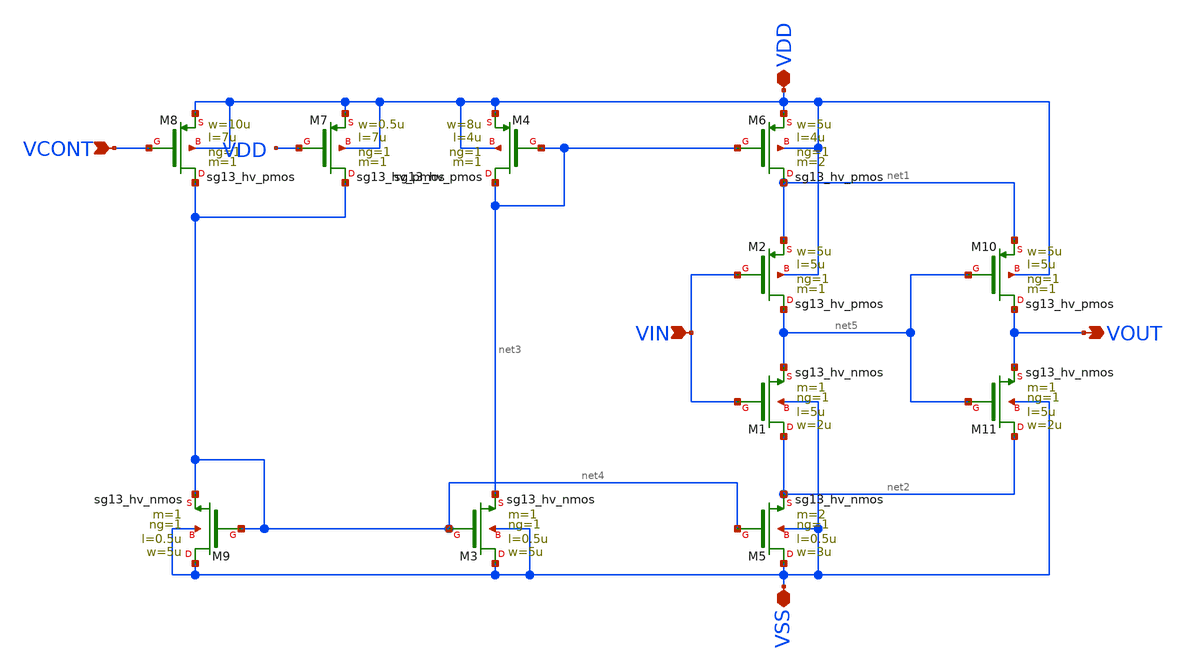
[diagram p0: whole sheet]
** sch_path: xschem/VCDL_v6p1.sch
**.subckt VCDL_v6p1 VIN VDD VSS VCONT VOUT
*.ipin VIN
*.iopin VDD
*.iopin VSS
*.ipin VCONT
*.opin VOUT
XM9 VSS net4 net4 VSS sg13_hv_nmos w=5u l=0.5u ng=1 m=1 mm_ok=1
XM3 VSS net4 net3 VSS sg13_hv_nmos w=5u l=0.5u ng=1 m=1 mm_ok=1
XM5 VSS net4 net2 VSS sg13_hv_nmos w=3u l=0.5u ng=1 m=2 mm_ok=1
XM8 net4 VCONT VDD VDD sg13_hv_pmos w=10u l=7u ng=1 m=1 mm_ok=1
XM4 net3 net3 VDD VDD sg13_hv_pmos w=8u l=4u ng=1 m=1 mm_ok=1
XM6 net1 net3 VDD VDD sg13_hv_pmos w=5u l=4u ng=1 m=2 mm_ok=1
XM2 net5 VIN net1 VDD sg13_hv_pmos w=5u l=5u ng=1 m=1 mm_ok=1
XM1 net2 VIN net5 VSS sg13_hv_nmos w=2u l=5u ng=1 m=1 mm_ok=1
XM7 net4 VDD VDD VDD sg13_hv_pmos w=0.5u l=7u ng=1 m=1 mm_ok=1
XM10 VOUT net5 net1 VDD sg13_hv_pmos w=5u l=5u ng=1 m=1 mm_ok=1
XM11 net2 net5 VOUT VSS sg13_hv_nmos w=2u l=5u ng=1 m=1 mm_ok=1
**.ends
.end
